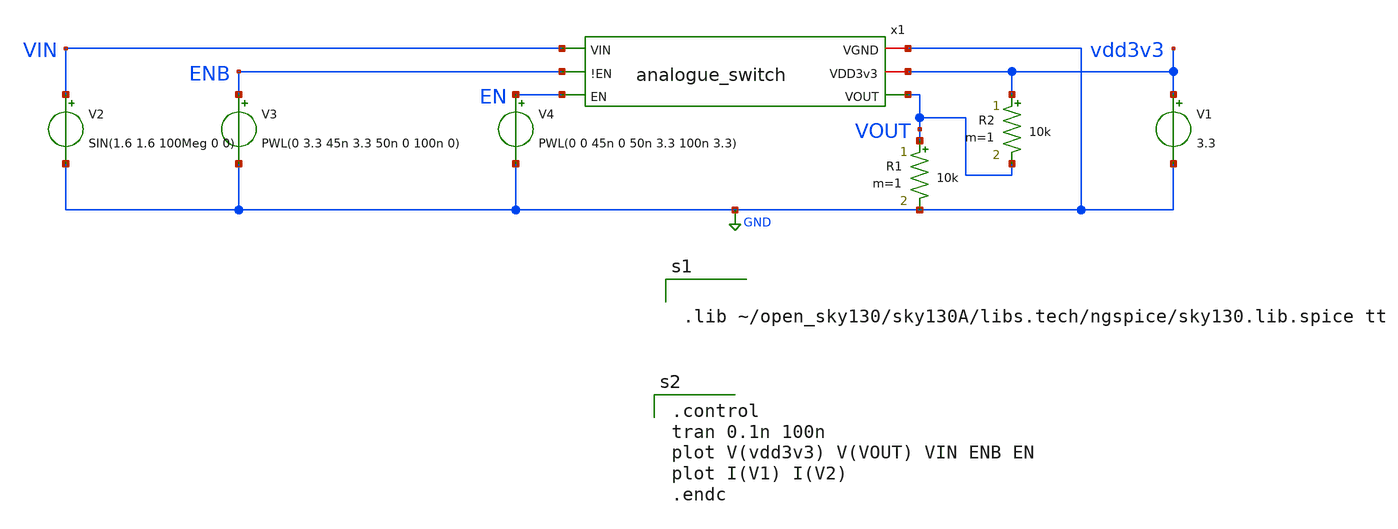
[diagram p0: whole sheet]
** sch_path: xschem/analog_mux/analogue_switch_tb.sch
**.subckt analogue_switch_tb
x1 GND vdd3v3 VIN ENB EN VOUT analogue_switch
V1 vdd3v3 GND 3.3
V2 VIN GND SIN(1.6 1.6 100Meg 0 0)
V3 ENB GND PWL(0 3.3 45n 3.3 50n 0 100n 0)
V4 EN GND PWL(0 0 45n 0 50n 3.3 100n 3.3)
R1 VOUT GND 10k m=1
R2 vdd3v3 VOUT 10k m=1
**** begin user architecture code


.lib ~/open_sky130/sky130A/libs.tech/ngspice/sky130.lib.spice tt


.control
tran 0.1n 100n
plot V(vdd3v3) V(VOUT) VIN ENB EN
plot I(V1) I(V2)
.endc

**** end user architecture code
**.ends

* expanding   symbol:  analogue_switch.sym # of pins=6
** sym_path: xschem/analog_mux/analogue_switch.sym
** sch_path: xschem/analog_mux/analogue_switch.sch
.subckt analogue_switch VGND VDD3v3 VIN !EN EN VOUT
*.ipin EN
*.ipin VIN
*.opin VOUT
*.ipin !EN
*.iopin VGND
*.iopin VDD3v3
XM2 mid !EN VIN VDD3v3 sky130_fd_pr__pfet_g5v0d10v5 L=0.5 W=15 nf=1 ad='int((nf+1)/2) * W/nf * 0.29'
+ as='int((nf+2)/2) * W/nf * 0.29' pd='2*int((nf+1)/2) * (W/nf + 0.29)' ps='2*int((nf+2)/2) * (W/nf + 0.29)'
+ nrd='0.29 / W' nrs='0.29 / W' sa=0 sb=0 sd=0 mult=2 m=2
XM1 VIN EN mid VGND sky130_fd_pr__nfet_03v3_nvt L=0.5 W=10 nf=1 ad='int((nf+1)/2) * W/nf * 0.29' as='int((nf+2)/2) * W/nf * 0.29'
+ pd='2*int((nf+1)/2) * (W/nf + 0.29)' ps='2*int((nf+2)/2) * (W/nf + 0.29)' nrd='0.29 / W' nrs='0.29 / W'
+ sa=0 sb=0 sd=0 mult=2 m=2
XM3 mid !EN VGND VGND sky130_fd_pr__nfet_03v3_nvt L=0.5 W=10 nf=1 ad='int((nf+1)/2) * W/nf * 0.29' as='int((nf+2)/2) * W/nf * 0.29'
+ pd='2*int((nf+1)/2) * (W/nf + 0.29)' ps='2*int((nf+2)/2) * (W/nf + 0.29)' nrd='0.29 / W' nrs='0.29 / W'
+ sa=0 sb=0 sd=0 mult=1 m=1
XM4 VOUT !EN mid VDD3v3 sky130_fd_pr__pfet_g5v0d10v5 L=0.5 W=15 nf=1 ad='int((nf+1)/2) * W/nf * 0.29'
+ as='int((nf+2)/2) * W/nf * 0.29' pd='2*int((nf+1)/2) * (W/nf + 0.29)' ps='2*int((nf+2)/2) * (W/nf + 0.29)'
+ nrd='0.29 / W' nrs='0.29 / W' sa=0 sb=0 sd=0 mult=2 m=2
XM5 mid EN VOUT VGND sky130_fd_pr__nfet_03v3_nvt L=0.5 W=10 nf=1 ad='int((nf+1)/2) * W/nf * 0.29' as='int((nf+2)/2) * W/nf * 0.29'
+ pd='2*int((nf+1)/2) * (W/nf + 0.29)' ps='2*int((nf+2)/2) * (W/nf + 0.29)' nrd='0.29 / W' nrs='0.29 / W'
+ sa=0 sb=0 sd=0 mult=2 m=2
.ends

.GLOBAL GND
.end
